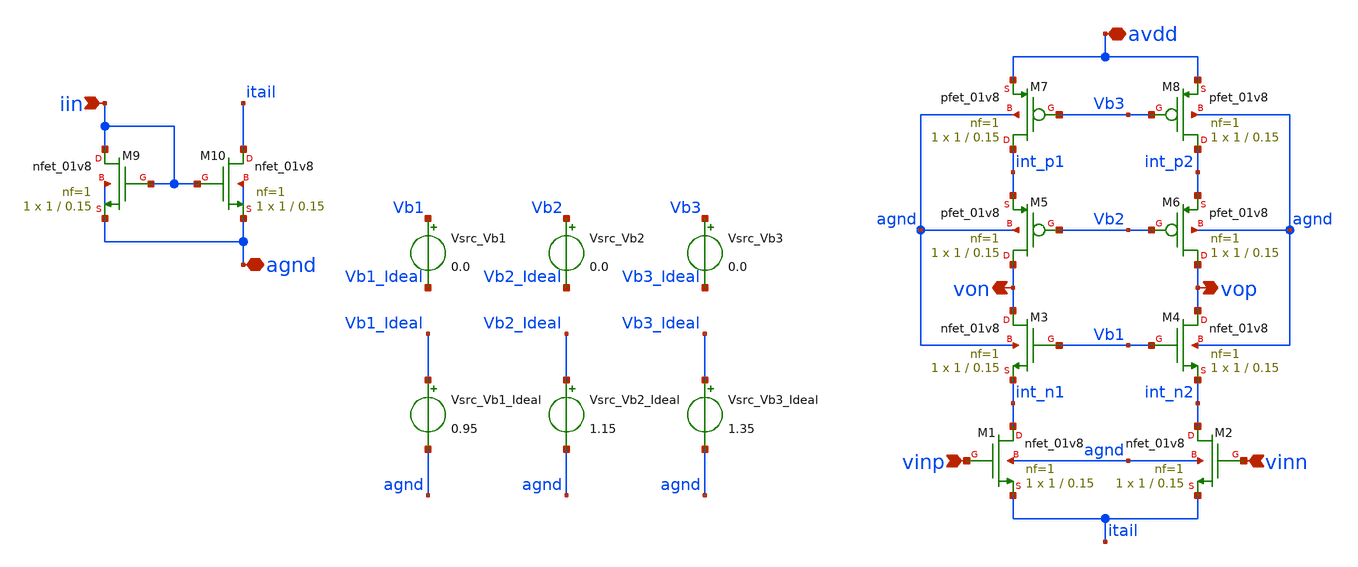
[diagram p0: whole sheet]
** sch_path: AMP/Final_Cascode.sch
**.subckt Final_Cascode avdd vinp vop agnd vinn von iin
*.iopin avdd
*.ipin vinp
*.opin vop
*.iopin agnd
*.ipin vinn
*.opin von
*.ipin iin
XM1 int_n1 vinp itail agnd sky130_fd_pr__nfet_01v8 L=0.15 W=1 nf=1 ad='int((nf+1)/2) * W/nf * 0.29' as='int((nf+2)/2) * W/nf * 0.29'
+ pd='2*int((nf+1)/2) * (W/nf + 0.29)' ps='2*int((nf+2)/2) * (W/nf + 0.29)' nrd='0.29 / W' nrs='0.29 / W'
+ sa=0 sb=0 sd=0 mult=1 m=1
XM5 von Vb2 int_p1 agnd sky130_fd_pr__pfet_01v8 L=0.15 W=1 nf=1 ad='int((nf+1)/2) * W/nf * 0.29' as='int((nf+2)/2) * W/nf * 0.29'
+ pd='2*int((nf+1)/2) * (W/nf + 0.29)' ps='2*int((nf+2)/2) * (W/nf + 0.29)' nrd='0.29 / W' nrs='0.29 / W'
+ sa=0 sb=0 sd=0 mult=1 m=1
XM2 int_n2 vinn itail agnd sky130_fd_pr__nfet_01v8 L=0.15 W=1 nf=1 ad='int((nf+1)/2) * W/nf * 0.29' as='int((nf+2)/2) * W/nf * 0.29'
+ pd='2*int((nf+1)/2) * (W/nf + 0.29)' ps='2*int((nf+2)/2) * (W/nf + 0.29)' nrd='0.29 / W' nrs='0.29 / W'
+ sa=0 sb=0 sd=0 mult=1 m=1
XM3 von Vb1 int_n1 agnd sky130_fd_pr__nfet_01v8 L=0.15 W=1 nf=1 ad='int((nf+1)/2) * W/nf * 0.29' as='int((nf+2)/2) * W/nf * 0.29'
+ pd='2*int((nf+1)/2) * (W/nf + 0.29)' ps='2*int((nf+2)/2) * (W/nf + 0.29)' nrd='0.29 / W' nrs='0.29 / W'
+ sa=0 sb=0 sd=0 mult=1 m=1
XM4 vop Vb1 int_n2 agnd sky130_fd_pr__nfet_01v8 L=0.15 W=1 nf=1 ad='int((nf+1)/2) * W/nf * 0.29' as='int((nf+2)/2) * W/nf * 0.29'
+ pd='2*int((nf+1)/2) * (W/nf + 0.29)' ps='2*int((nf+2)/2) * (W/nf + 0.29)' nrd='0.29 / W' nrs='0.29 / W'
+ sa=0 sb=0 sd=0 mult=1 m=1
XM6 vop Vb2 int_p2 agnd sky130_fd_pr__pfet_01v8 L=0.15 W=1 nf=1 ad='int((nf+1)/2) * W/nf * 0.29' as='int((nf+2)/2) * W/nf * 0.29'
+ pd='2*int((nf+1)/2) * (W/nf + 0.29)' ps='2*int((nf+2)/2) * (W/nf + 0.29)' nrd='0.29 / W' nrs='0.29 / W'
+ sa=0 sb=0 sd=0 mult=1 m=1
XM7 int_p1 Vb3 avdd agnd sky130_fd_pr__pfet_01v8 L=0.15 W=1 nf=1 ad='int((nf+1)/2) * W/nf * 0.29' as='int((nf+2)/2) * W/nf * 0.29'
+ pd='2*int((nf+1)/2) * (W/nf + 0.29)' ps='2*int((nf+2)/2) * (W/nf + 0.29)' nrd='0.29 / W' nrs='0.29 / W'
+ sa=0 sb=0 sd=0 mult=1 m=1
XM8 int_p2 Vb3 avdd agnd sky130_fd_pr__pfet_01v8 L=0.15 W=1 nf=1 ad='int((nf+1)/2) * W/nf * 0.29' as='int((nf+2)/2) * W/nf * 0.29'
+ pd='2*int((nf+1)/2) * (W/nf + 0.29)' ps='2*int((nf+2)/2) * (W/nf + 0.29)' nrd='0.29 / W' nrs='0.29 / W'
+ sa=0 sb=0 sd=0 mult=1 m=1
XM9 iin iin agnd agnd sky130_fd_pr__nfet_01v8 L=0.15 W=1 nf=1 ad='int((nf+1)/2) * W/nf * 0.29' as='int((nf+2)/2) * W/nf * 0.29'
+ pd='2*int((nf+1)/2) * (W/nf + 0.29)' ps='2*int((nf+2)/2) * (W/nf + 0.29)' nrd='0.29 / W' nrs='0.29 / W'
+ sa=0 sb=0 sd=0 mult=1 m=1
XM10 itail iin agnd agnd sky130_fd_pr__nfet_01v8 L=0.15 W=1 nf=1 ad='int((nf+1)/2) * W/nf * 0.29' as='int((nf+2)/2) * W/nf * 0.29'
+ pd='2*int((nf+1)/2) * (W/nf + 0.29)' ps='2*int((nf+2)/2) * (W/nf + 0.29)' nrd='0.29 / W' nrs='0.29 / W'
+ sa=0 sb=0 sd=0 mult=1 m=1
Vsrc_Vb3_Ideal Vb3_Ideal agnd 1.35
Vsrc_Vb2_Ideal Vb2_Ideal agnd 1.15
Vsrc_Vb1_Ideal Vb1_Ideal agnd 0.95
Vsrc_Vb3 Vb3 Vb3_Ideal 0.0
Vsrc_Vb2 Vb2 Vb2_Ideal 0.0
Vsrc_Vb1 Vb1 Vb1_Ideal 0.0
**.ends
.end
